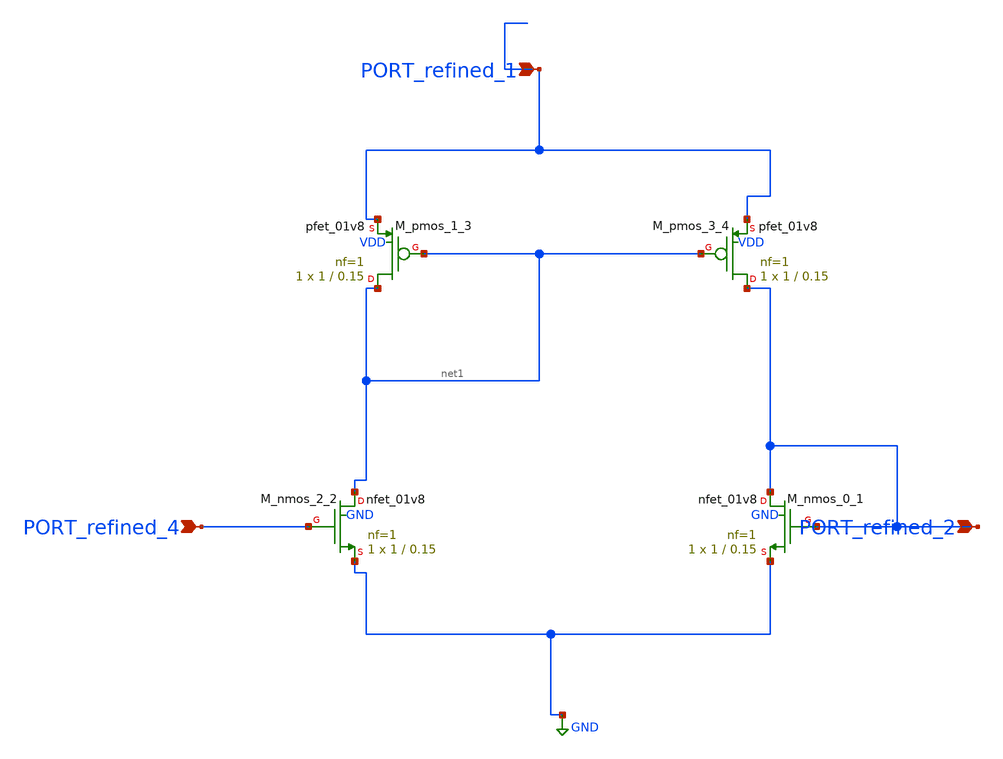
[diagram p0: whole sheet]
** sch_path: schematics/10_29292_jics_v15i1_101_03_001.sch
**.subckt 10_29292_jics_v15i1_101_03_001 PORT_refined_1 PORT_refined_2 PORT_refined_4
*.ipin PORT_refined_1
*.ipin PORT_refined_2
*.ipin PORT_refined_4
XM_nmos_0_1 PORT_refined_2 PORT_refined_2 GND GND sky130_fd_pr__nfet_01v8 L=0.15 W=1 nf=1 ad='int((1 + 1)/2) * 1 / 1 * 0.29'
+ as='int((1 + 2)/2) * 1 / 1 * 0.29' pd='2*int((1 + 1)/2) * (1 / 1 + 0.29)' ps='2*int((1 + 2)/2) * (1 / 1 + 0.29)'
+ nrd='0.29 / 1 ' nrs='0.29 / 1 ' sa=0 sb=0 sd=0 mult=1 m=1
XM_nmos_2_2 net1 PORT_refined_4 GND GND sky130_fd_pr__nfet_01v8 L=0.15 W=1 nf=1 ad='int((1 + 1)/2) * 1 / 1 * 0.29'
+ as='int((1 + 2)/2) * 1 / 1 * 0.29' pd='2*int((1 + 1)/2) * (1 / 1 + 0.29)' ps='2*int((1 + 2)/2) * (1 / 1 + 0.29)'
+ nrd='0.29 / 1 ' nrs='0.29 / 1 ' sa=0 sb=0 sd=0 mult=1 m=1
XM_pmos_1_3 net1 net1 PORT_refined_1 VDD sky130_fd_pr__pfet_01v8 L=0.15 W=1 nf=1 ad='int((1 + 1)/2) * 1 / 1 * 0.29'
+ as='int((1 + 2)/2) * 1 / 1 * 0.29' pd='2*int((1 + 1)/2) * (1 / 1 + 0.29)' ps='2*int((1 + 2)/2) * (1 / 1 + 0.29)'
+ nrd='0.29 / 1 ' nrs='0.29 / 1 ' sa=0 sb=0 sd=0 mult=1 m=1
XM_pmos_3_4 PORT_refined_2 net1 PORT_refined_1 VDD sky130_fd_pr__pfet_01v8 L=0.15 W=1 nf=1 ad='int((1 + 1)/2) * 1 / 1 * 0.29'
+ as='int((1 + 2)/2) * 1 / 1 * 0.29' pd='2*int((1 + 1)/2) * (1 / 1 + 0.29)' ps='2*int((1 + 2)/2) * (1 / 1 + 0.29)'
+ nrd='0.29 / 1 ' nrs='0.29 / 1 ' sa=0 sb=0 sd=0 mult=1 m=1
**.ends
.GLOBAL GND
.end
